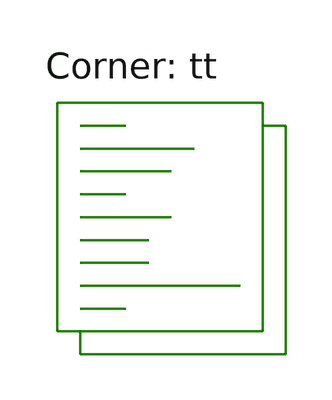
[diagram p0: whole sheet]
** sch_path: xschem/signal_test-tb.sch
**.subckt signal_test-tb
**** begin user architecture code
.lib $::SKYWATER_MODELS/sky130.lib.spice tt



  .option wnflag=1
  .option safecurrents
  ********************Static Voltage Sources***************************
  Vddh vddh gnd dc 5

  V52 v[52] gnd dc 3.8499
  v0 v[0] gnd dc 0.874109
  ********************Dynamic Voltage Sources***************************
  *******Calculation**********
  .param base_f=100e3 base_t={1/base_f} base_th={base_t/2} base_d={base_th}
  .param d2_th ={base_th} d2_t={d1_th}
  .param d1_th ={4*d2_th} d1_t={d0_th}
  .param d0_th ={4*d1_th} d0_t={4*d0_th}

  .param d20_d ={0} d21_d={1*d2_th} d22_d={2*d2_th} d23_d={3*d2_th}
  .param d10_d ={0} d11_d={1*d1_th} d12_d={2*d1_th} d13_d={3*d1_th}
  .param d00_d ={0} d01_d={1*d0_th} d02_d={2*d0_th} d03_d={3*d0_th}
  *******Signals**********
  .param vhi=5.5
  Vd00 d0[0] gnd pulse(0 {vhi} {d00_d} 1n 1n {d0_th} {d0_t})
  Vd01 d0[1] gnd pulse(0 {vhi} {d01_d} 1n 1n {d0_th} {d0_t})
  Vd02 d0[2] gnd pulse(0 {vhi} {d02_d} 1n 1n {d0_th} {d0_t})
  Vd03 d0[3] gnd pulse(0 {vhi} {d03_d} 1n 1n {d0_th} {d0_t})

  Vd10 d1[0] gnd pulse(0 {vhi} {d10_d} 1n 1n {d1_th} {d1_t})
  Vd11 d1[1] gnd pulse(0 {vhi} {d11_d} 1n 1n {d1_th} {d1_t})
  Vd12 d1[2] gnd pulse(0 {vhi} {d12_d} 1n 1n {d1_th} {d1_t})
  Vd13 d1[3] gnd pulse(0 {vhi} {d13_d} 1n 1n {d1_th} {d1_t})

  Vd20 d2[0] gnd pulse(0 {vhi} {d20_d} 1n 1n {d2_th} {d2_t})
  Vd21 d2[1] gnd pulse(0 {vhi} {d21_d} 1n 1n {d2_th} {d2_t})
  Vd22 d2[2] gnd pulse(0 {vhi} {d22_d} 1n 1n {d2_th} {d2_t})
  Vd23 d2[3] gnd pulse(0 {vhi} {d23_d} 1n 1n {d2_th} {d2_t})
  ********************Simulation Commands*****************************
  .control
     reset
     save all
     tran 1n 500u
     write signal_test-tb.raw
     set appendwrite
*    quit 0
  .endc



**** end user architecture code
**.ends
.end
